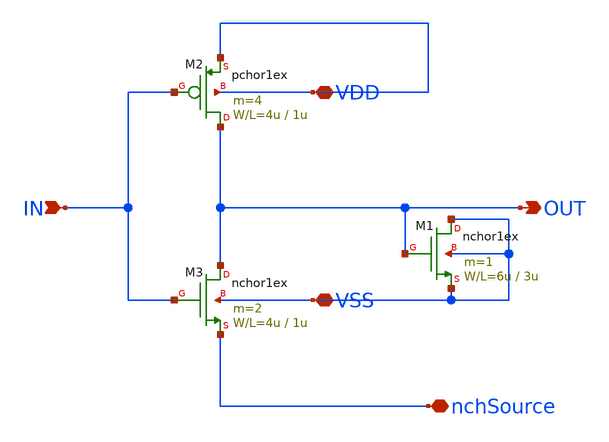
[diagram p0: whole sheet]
** sch_path: design/xschem/VCO/SA_VCO_INV.sch
**.subckt SA_VCO_INV nchSource IN OUT VDD VSS
*.iopin nchSource
*.ipin IN
*.opin OUT
*.iopin VDD
*.iopin VSS
M1 VSS OUT VSS VSS nchor1ex L=3u W=6u m=1
M2 OUT IN VDD VDD pchor1ex L=1u W=4u m=4
M3 OUT IN nchSource VSS nchor1ex L=1u W=4u m=2
**.ends
.end
